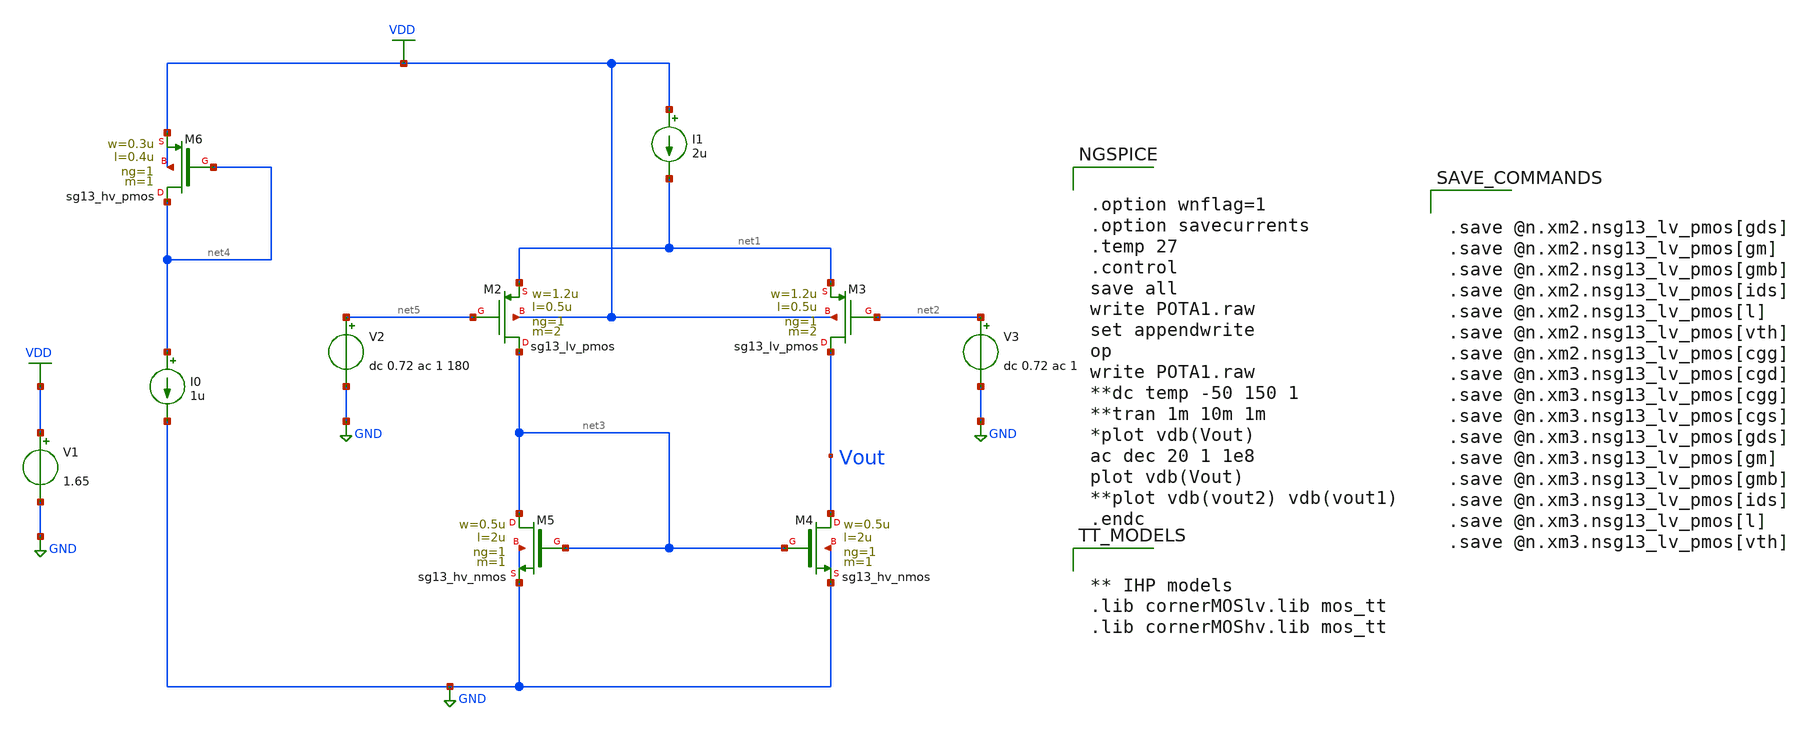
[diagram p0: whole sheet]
** sch_path: Design Files/RAMP/OTA/POTA1.sch
**.subckt POTA1
XM2 net3 net5 net1 VDD sg13_lv_pmos w=1.2u l=0.5u ng=1 m=2 mm_ok=1
XM3 Vout net2 net1 VDD sg13_lv_pmos w=1.2u l=0.5u ng=1 m=2 mm_ok=1
XM4 Vout net3 GND GND sg13_hv_nmos w=0.5u l=2u ng=1 m=1 mm_ok=1
XM5 net3 net3 GND GND sg13_hv_nmos w=0.5u l=2u ng=1 m=1 mm_ok=1
XM6 net4 net4 VDD VDD sg13_hv_pmos w=0.3u l=0.4u ng=1 m=1 mm_ok=1
I0 net4 GND 1u
V1 VDD GND 1.65
V2 net5 GND dc 0.72 ac 1 180
V3 net2 GND dc 0.72 ac 1
I1 VDD net1 2u
**** begin user architecture code


.option wnflag=1
.option savecurrents
.temp 27
.control
save all
write POTA1.raw
set appendwrite
op
write POTA1.raw
**dc temp -50 150 1
**tran 1m 10m 1m
*plot vdb(Vout)
ac dec 20 1 1e8
plot vdb(Vout)
**plot vdb(vout2) vdb(vout1)
.endc




** IHP models
.lib cornerMOSlv.lib mos_tt
.lib cornerMOShv.lib mos_tt




.save @n.xm2.nsg13_lv_pmos[gds]
.save @n.xm2.nsg13_lv_pmos[gm]
.save @n.xm2.nsg13_lv_pmos[gmb]
.save @n.xm2.nsg13_lv_pmos[ids]
.save @n.xm2.nsg13_lv_pmos[l]
.save @n.xm2.nsg13_lv_pmos[vth]
.save @n.xm2.nsg13_lv_pmos[cgg]
.save @n.xm3.nsg13_lv_pmos[cgd]
.save @n.xm3.nsg13_lv_pmos[cgg]
.save @n.xm3.nsg13_lv_pmos[cgs]
.save @n.xm3.nsg13_lv_pmos[gds]
.save @n.xm3.nsg13_lv_pmos[gm]
.save @n.xm3.nsg13_lv_pmos[gmb]
.save @n.xm3.nsg13_lv_pmos[ids]
.save @n.xm3.nsg13_lv_pmos[l]
.save @n.xm3.nsg13_lv_pmos[vth]


**** end user architecture code
**.ends
.GLOBAL GND
.GLOBAL VDD
.end
